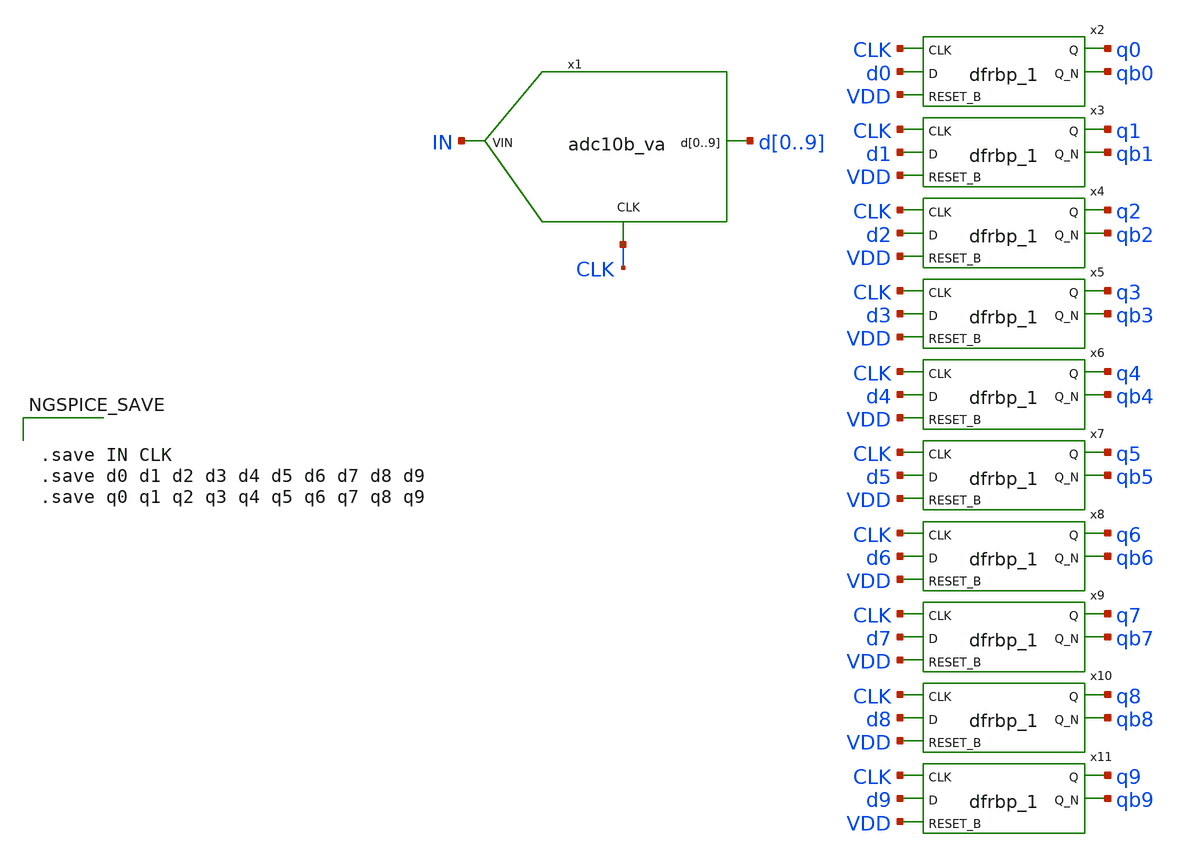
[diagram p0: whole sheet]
** sch_path: xschem/signal_test_2.sch
.lib $::SKYWATER_MODELS/sky130.lib.spice tt
.include $::SKYWATER_STDCELLS/sky130_fd_sc_hd.spice

**.subckt signal_test_2
x1 IN CLK d0 d1 d2 d3 d4 d5 d6 d7 d8 d9 adc10b_va
x2 CLK d0 VDD GND GND VDD VDD q0 qb0 sky130_fd_sc_hd__dfrbp_1
x3 CLK d1 VDD GND GND VDD VDD q1 qb1 sky130_fd_sc_hd__dfrbp_1
x4 CLK d2 VDD GND GND VDD VDD q2 qb2 sky130_fd_sc_hd__dfrbp_1
x5 CLK d3 VDD GND GND VDD VDD q3 qb3 sky130_fd_sc_hd__dfrbp_1
x6 CLK d4 VDD GND GND VDD VDD q4 qb4 sky130_fd_sc_hd__dfrbp_1
x7 CLK d5 VDD GND GND VDD VDD q5 qb5 sky130_fd_sc_hd__dfrbp_1
x8 CLK d6 VDD GND GND VDD VDD q6 qb6 sky130_fd_sc_hd__dfrbp_1
x9 CLK d7 VDD GND GND VDD VDD q7 qb7 sky130_fd_sc_hd__dfrbp_1
x10 CLK d8 VDD GND GND VDD VDD q8 qb8 sky130_fd_sc_hd__dfrbp_1
x11 CLK d9 VDD GND GND VDD VDD q9 qb9 sky130_fd_sc_hd__dfrbp_1
**** begin user architecture code



  *.options wnflag=0 bypass=1
  .option wnflag=1
  .option safecurrents
  *.option klu
  .options solver=klu nomod
  .options method=gear rawfile=binary
  .options reltol=1e-2

  .subckt adc10b_va in clk d0 d1 d2 d3 d4 d5 d6 d7 d8 d9
  N1 in clk d0 d1 d2 d3 d4 d5 d6 d7 d8 d9 adc_model
  .ends
  .model adc_model adc10bit
  ********************Static Voltage Sources***************************
  Vin in gnd SIN(0.9 0.9 9.95k)
  Vclk clk gnd pulse(1.8 0 10n 10n 0 5u 10u)

  VDD VDD gnd 1.8
  ********************Simulation Commands*****************************
  .control
     reset
     pre_osdi $THESIS_WS/verilogA/adc10bit.osdi
     set num_threads=8
     tran 10n 1m
     write signal_test_2-tb.raw
  .endc





.save IN CLK
.save d0 d1 d2 d3 d4 d5 d6 d7 d8 d9
.save q0 q1 q2 q3 q4 q5 q6 q7 q8 q9


**** end user architecture code
**.ends
.end
